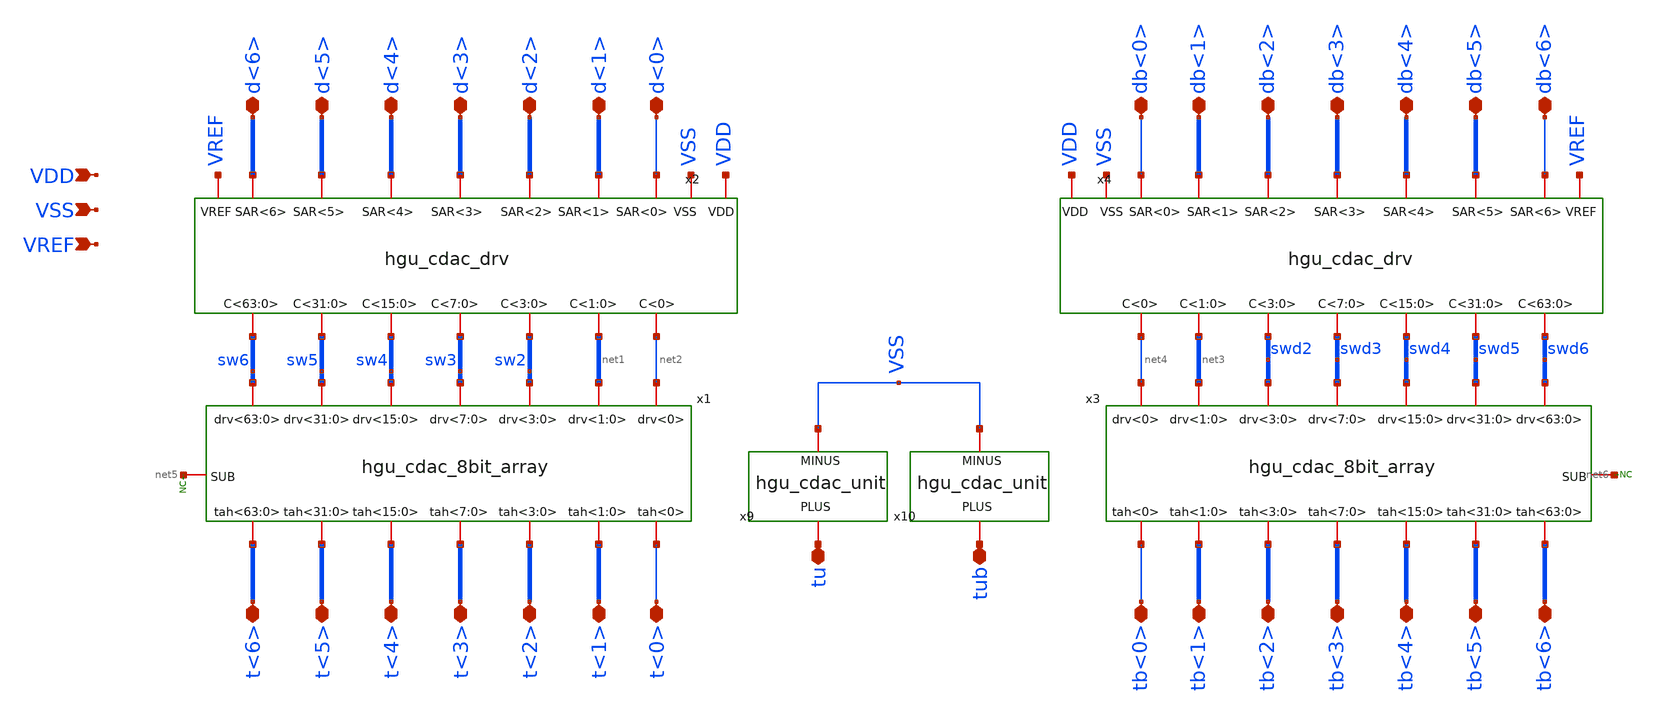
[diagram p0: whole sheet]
** sch_path: hgu/xschem/hgu_cdac_half.sch
**.subckt hgu_cdac_half d<6> d<5> d<4> d<3> d<2> d<1> d<0> db<6> db<5> db<4> db<3> db<2> db<1> db<0>
*+ VSS VREF t<6> t<5> t<4> t<3> t<2> t<1> t<0> tb<6> tb<5> tb<4> tb<3> tb<2> tb<1> tb<0> tu tub VDD
*.iopin d<6>
*.iopin d<5>
*.iopin d<4>
*.iopin d<3>
*.iopin d<2>
*.iopin d<1>
*.iopin d<0>
*.iopin db<6>
*.iopin db<5>
*.iopin db<4>
*.iopin db<3>
*.iopin db<2>
*.iopin db<1>
*.iopin db<0>
*.ipin VSS
*.ipin VREF
*.iopin t<6>
*.iopin t<5>
*.iopin t<4>
*.iopin t<3>
*.iopin t<2>
*.iopin t<1>
*.iopin t<0>
*.iopin tb<6>
*.iopin tb<5>
*.iopin tb<4>
*.iopin tb<3>
*.iopin tb<2>
*.iopin tb<1>
*.iopin tb<0>
*.iopin tu
*.iopin tub
*.ipin VDD
x1 sw5 net1 net2 sw2 sw6 sw4 sw3 t<6> t<5> t<4> t<3> t<2> t<1> t<0> net5 hgu_cdac_8bit_array
x2 VREF d<4> d<1> d<2> d<3> d<5> d<6> d<0> sw2 sw3 sw4 sw5 net2 net1 sw6 VSS VDD hgu_cdac_drv
x3 swd5 net3 net4 swd2 swd6 swd4 swd3 tb<6> tb<5> tb<4> tb<3> tb<2> tb<1> tb<0> net6
+ hgu_cdac_8bit_array
x4 VREF db<4> db<1> db<2> db<3> db<5> db<6> db<0> swd2 swd3 swd4 swd5 net4 net3 swd6 VSS VDD
+ hgu_cdac_drv
x9 tu VSS hgu_cdac_unit
x10 tub VSS hgu_cdac_unit
* noconn #net5
* noconn #net6
**.ends
.end
